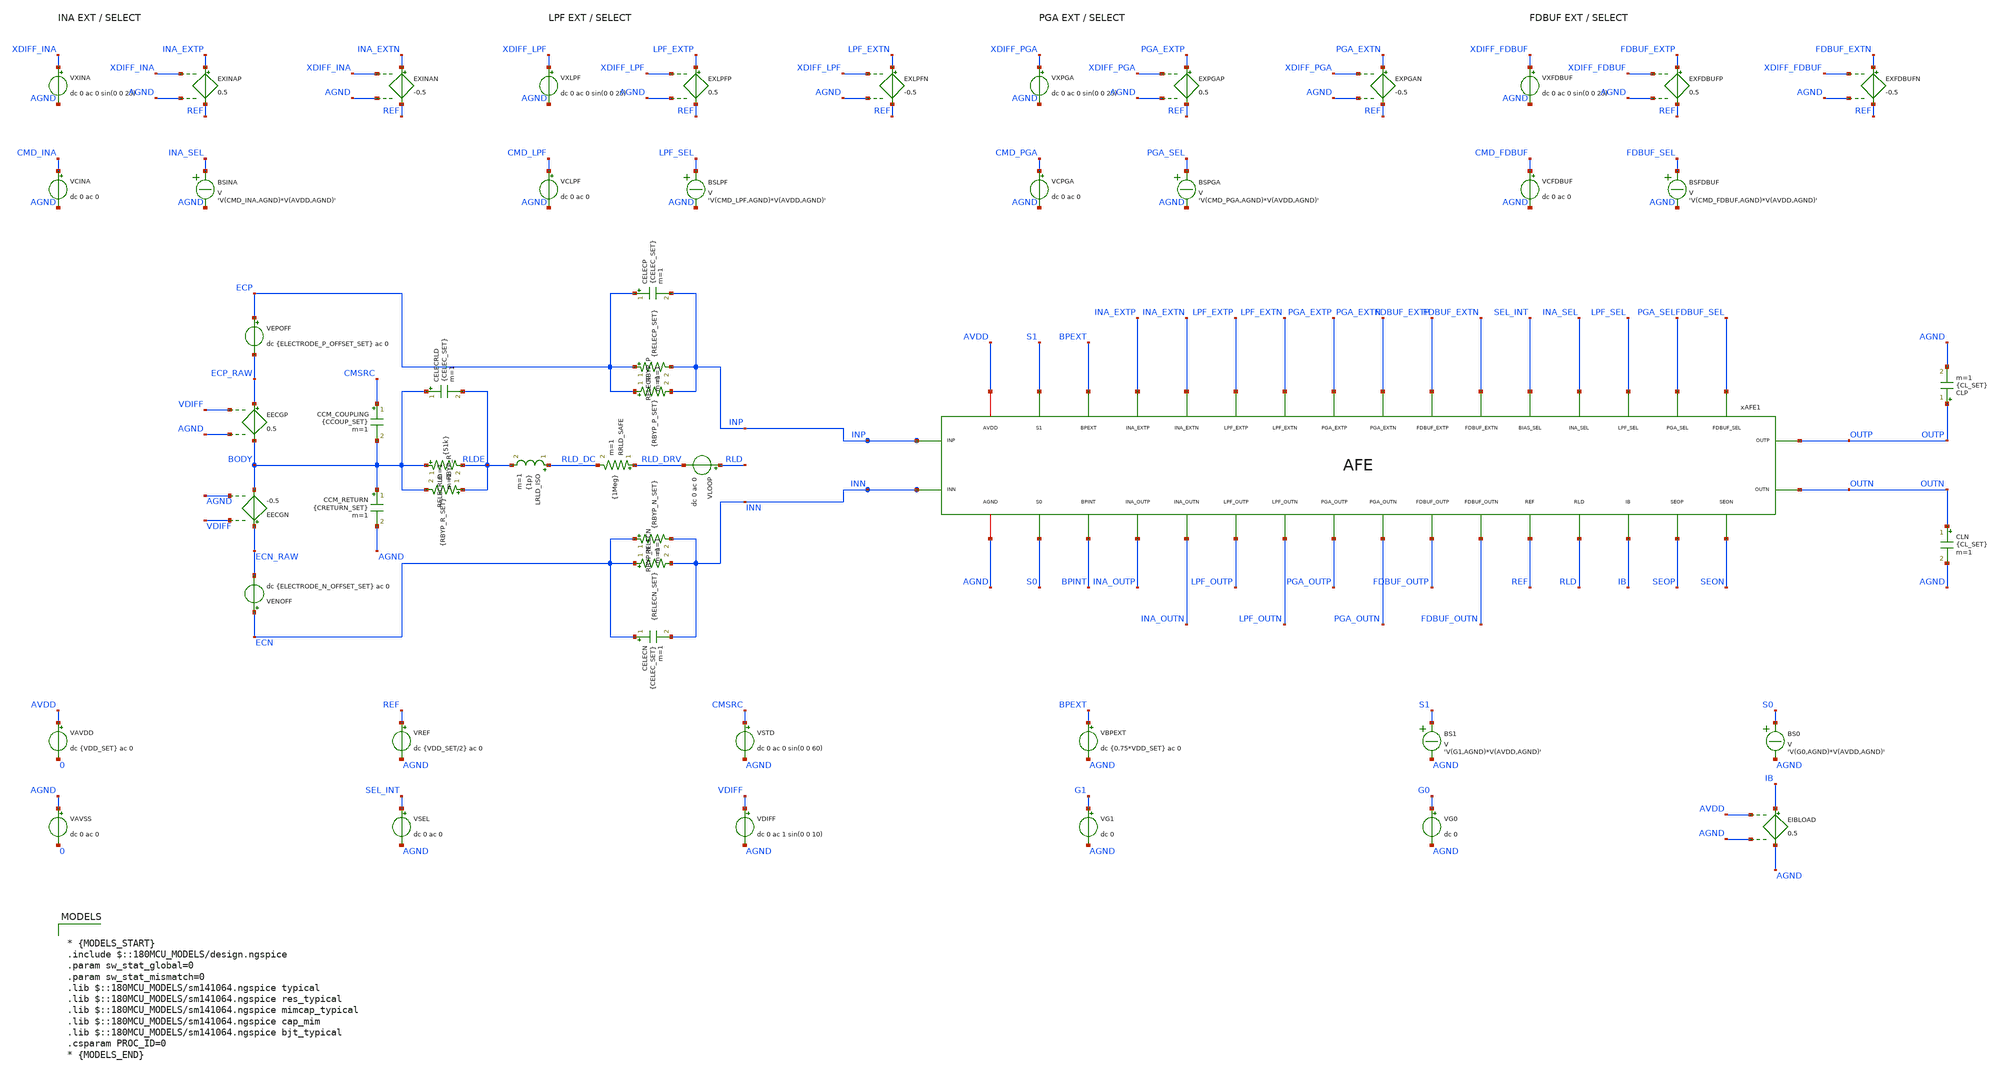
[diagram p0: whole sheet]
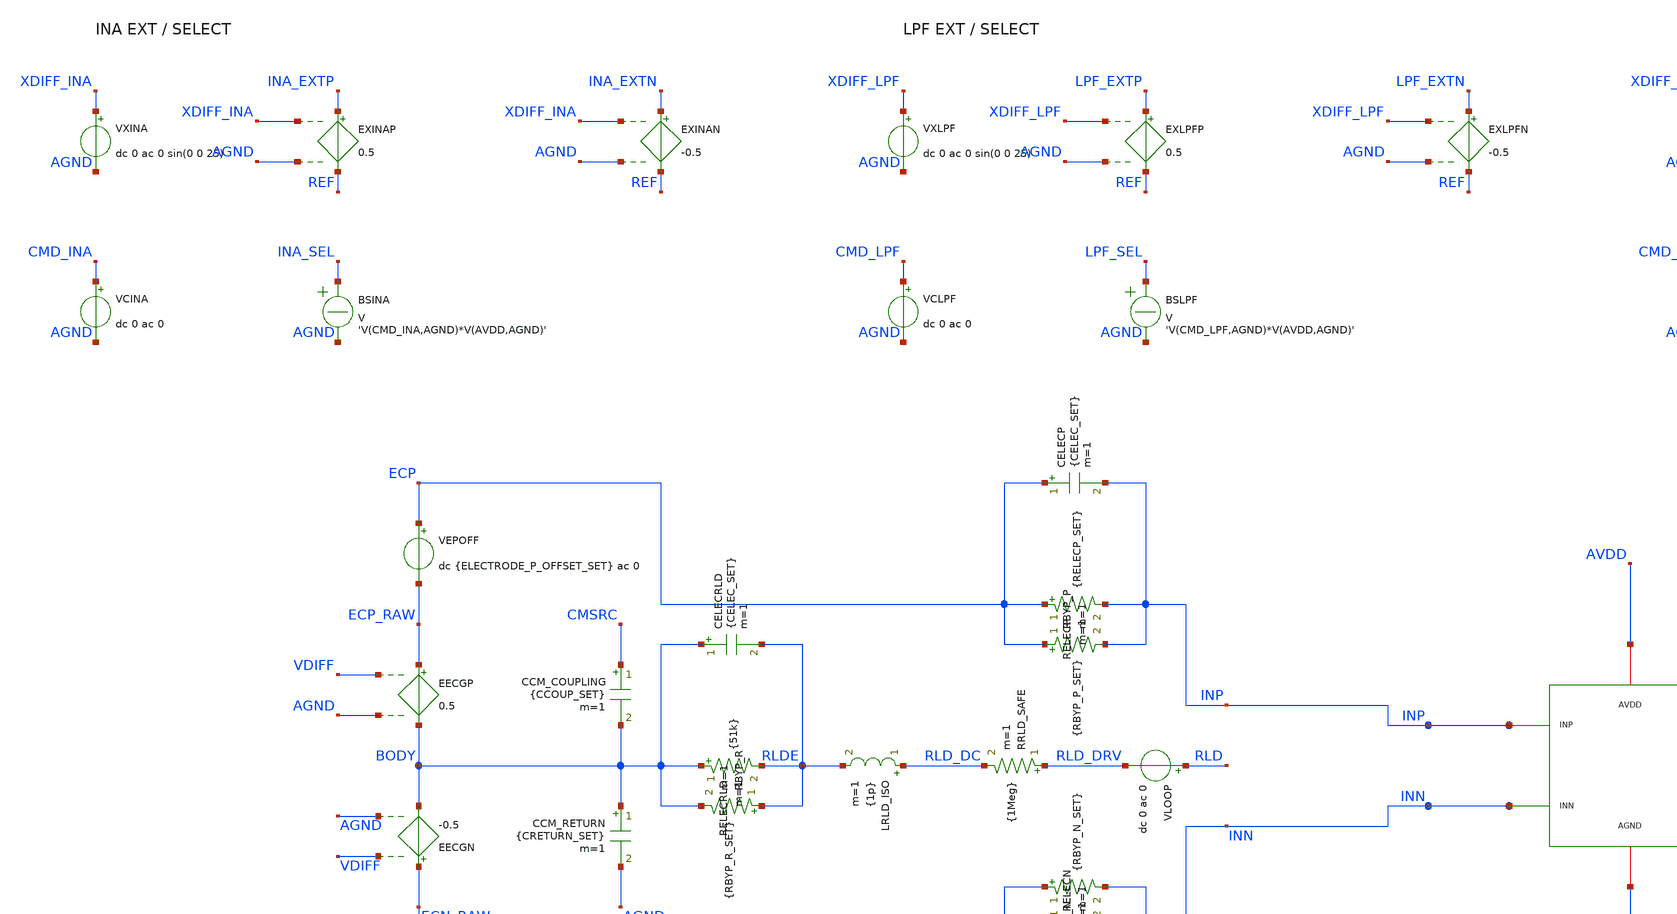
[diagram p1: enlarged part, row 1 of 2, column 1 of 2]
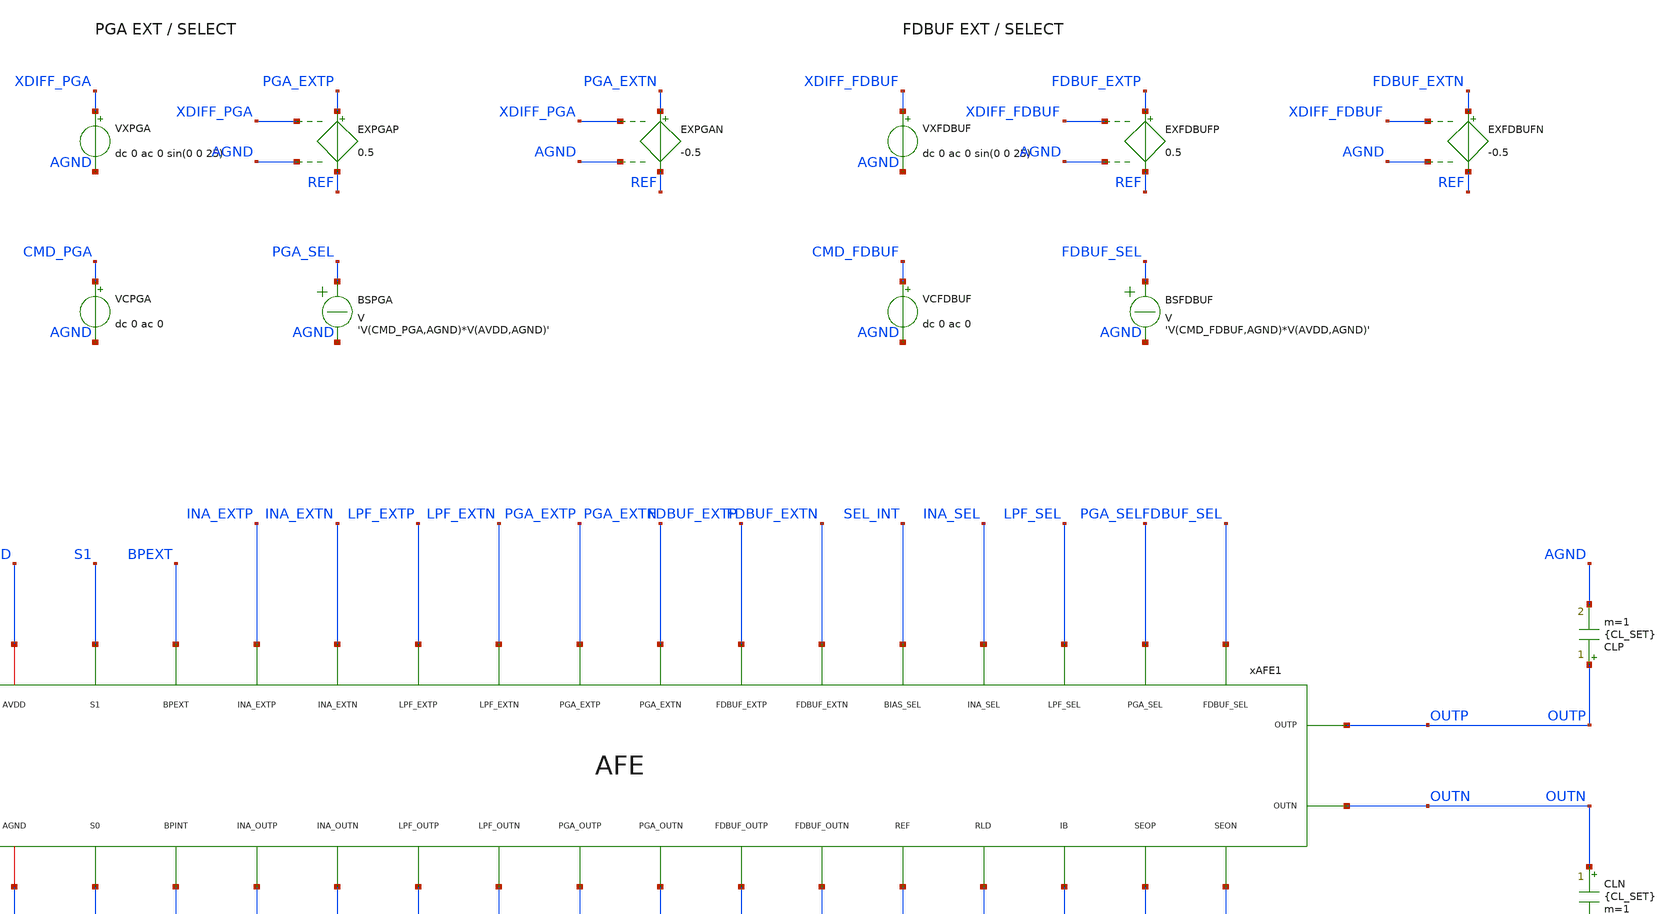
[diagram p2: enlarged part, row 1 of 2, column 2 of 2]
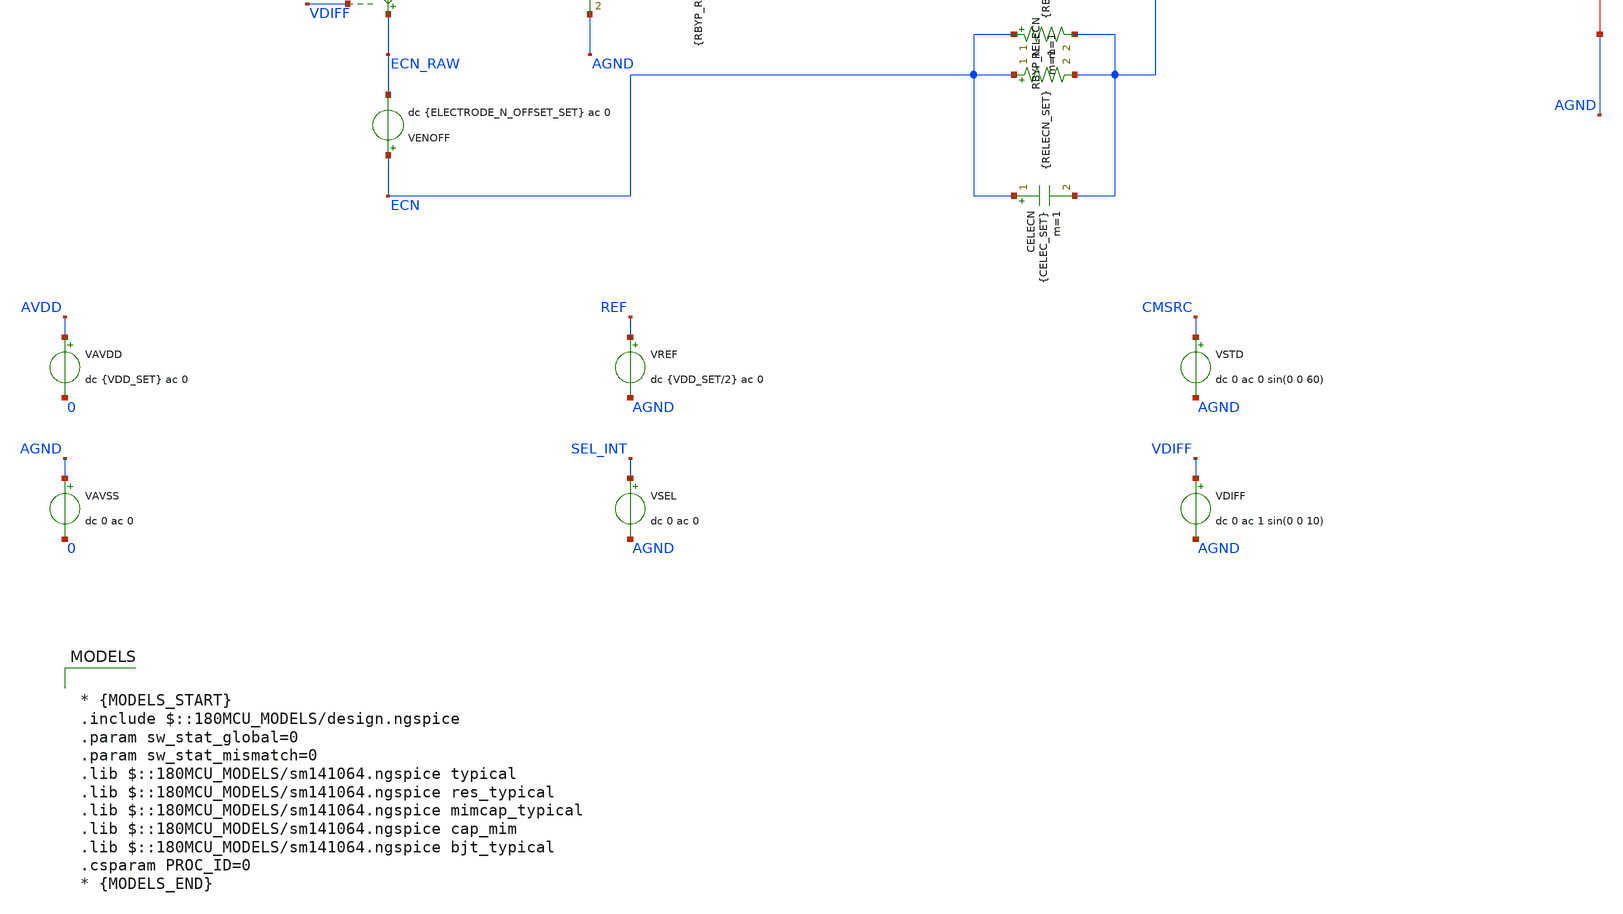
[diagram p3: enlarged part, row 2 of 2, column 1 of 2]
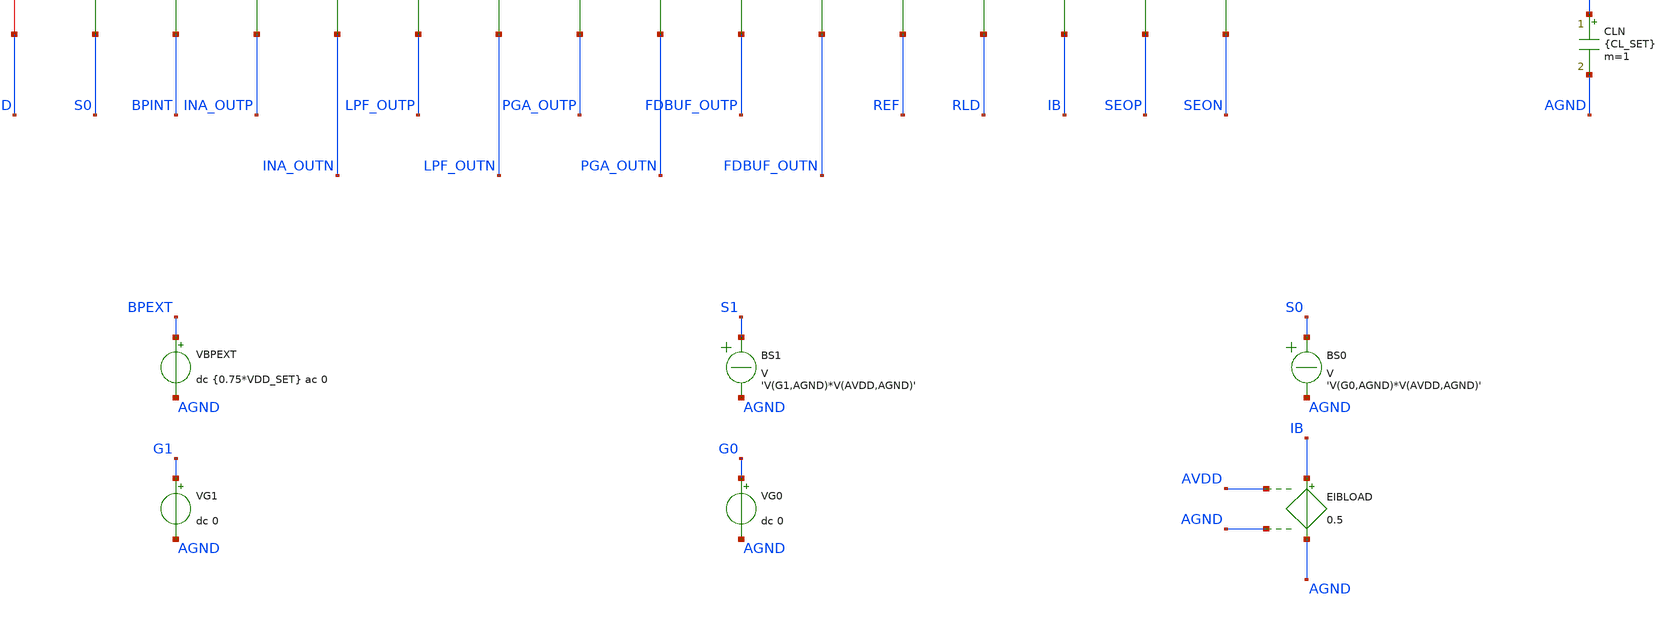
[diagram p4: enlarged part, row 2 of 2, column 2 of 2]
** sch_path: Design_Files/IC Design/Testbench/AFE_BLOCKS/AFE/AFE_TB_PVT_NOM.sch
**.subckt AFE_TB_PVT_NOM
VXINA XDIFF_INA AGND dc 0 ac 0 sin(0 0 25)
EXINAP INA_EXTP REF XDIFF_INA AGND 0.5
EXINAN INA_EXTN REF XDIFF_INA AGND -0.5
VCINA CMD_INA AGND dc 0 ac 0
BSINA INA_SEL AGND V = 'V(CMD_INA,AGND)*V(AVDD,AGND)'
VXLPF XDIFF_LPF AGND dc 0 ac 0 sin(0 0 25)
EXLPFP LPF_EXTP REF XDIFF_LPF AGND 0.5
EXLPFN LPF_EXTN REF XDIFF_LPF AGND -0.5
VCLPF CMD_LPF AGND dc 0 ac 0
BSLPF LPF_SEL AGND V = 'V(CMD_LPF,AGND)*V(AVDD,AGND)'
VXPGA XDIFF_PGA AGND dc 0 ac 0 sin(0 0 25)
EXPGAP PGA_EXTP REF XDIFF_PGA AGND 0.5
EXPGAN PGA_EXTN REF XDIFF_PGA AGND -0.5
VCPGA CMD_PGA AGND dc 0 ac 0
BSPGA PGA_SEL AGND V = 'V(CMD_PGA,AGND)*V(AVDD,AGND)'
VXFDBUF XDIFF_FDBUF AGND dc 0 ac 0 sin(0 0 25)
EXFDBUFP FDBUF_EXTP REF XDIFF_FDBUF AGND 0.5
EXFDBUFN FDBUF_EXTN REF XDIFF_FDBUF AGND -0.5
VCFDBUF CMD_FDBUF AGND dc 0 ac 0
BSFDBUF FDBUF_SEL AGND V = 'V(CMD_FDBUF,AGND)*V(AVDD,AGND)'
EECGP ECP_RAW BODY VDIFF AGND 0.5
EECGN ECN_RAW BODY VDIFF AGND -0.5
VLOOP RLD RLD_DRV dc 0 ac 0
.save i(vloop)
CCM_COUPLING CMSRC BODY {CCOUP_SET} m=1
RELECP ECP INP {RELECP_SET} m=1
RELECN ECN INN {RELECN_SET} m=1
CELECP ECP INP {CELEC_SET} m=1
CELECN ECN INN {CELEC_SET} m=1
RRLD_SAFE RLD_DRV RLD_DC {1Meg} m=1
RELECRLD BODY RLDE {51k} m=1
CELECRLD BODY RLDE {CELEC_SET} m=1
VEPOFF ECP ECP_RAW dc {ELECTRODE_P_OFFSET_SET} ac 0
VENOFF ECN ECN_RAW dc {ELECTRODE_N_OFFSET_SET} ac 0
CCM_RETURN BODY AGND {CRETURN_SET} m=1
RBYP_P ECP INP {RBYP_P_SET} m=1
RBYP_N ECN INN {RBYP_N_SET} m=1
RBYP_R RLDE BODY {RBYP_R_SET} m=1
LRLD_ISO RLD_DC RLDE {1p} m=1
xAFE1 FDBUF_SEL LPF_SEL SEL_INT PGA_SEL AVDD INA_SEL AGND FDBUF_OUTP BPINT LPF_OUTP PGA_OUTP
+ INA_OUTP INA_OUTN LPF_OUTN INP BPEXT FDBUF_OUTN PGA_OUTN FDBUF_EXTP LPF_EXTP INN PGA_EXTP INA_EXTP PGA_EXTN
+ INA_EXTN FDBUF_EXTN LPF_EXTN OUTP REF OUTN S1 SEOP IB S0 SEON RLD AFE
VAVDD AVDD 0 dc {VDD_SET} ac 0
.save i(vavdd)
VAVSS AGND 0 dc 0 ac 0
VREF REF AGND dc {VDD_SET/2} ac 0
VSEL SEL_INT AGND dc 0 ac 0
VSTD CMSRC AGND dc 0 ac 0 sin(0 0 60)
VDIFF VDIFF AGND dc 0 ac 1 sin(0 0 10)
VBPEXT BPEXT AGND dc {0.75*VDD_SET} ac 0
VG1 G1 AGND dc 0
VG0 G0 AGND dc 0
BS1 S1 AGND V = 'V(G1,AGND)*V(AVDD,AGND)'
BS0 S0 AGND V = 'V(G0,AGND)*V(AVDD,AGND)'
CLP OUTP AGND {CL_SET} m=1
CLN OUTN AGND {CL_SET} m=1
EIBLOAD IB AGND AVDD AGND 0.5
**** begin user architecture code

* {MODELS_START}
.include $::180MCU_MODELS/design.ngspice
.param sw_stat_global=0
.param sw_stat_mismatch=0
.lib $::180MCU_MODELS/sm141064.ngspice typical
.lib $::180MCU_MODELS/sm141064.ngspice res_typical
.lib $::180MCU_MODELS/sm141064.ngspice mimcap_typical
.lib $::180MCU_MODELS/sm141064.ngspice cap_mim
.lib $::180MCU_MODELS/sm141064.ngspice bjt_typical
.csparam PROC_ID=0
* {MODELS_END}




* {SETUP_START}
.param VDD_SET=3.3
.param TEMP_SET=27
.param CL_SET=60p
.param RELECP_SET=51k
.param RELECN_SET=51k
.param CELEC_SET=47n
.param CCOUP_SET=100p
.param CRETURN_SET=100p
.param ELECTRODE_P_OFFSET_SET=0
.param ELECTRODE_N_OFFSET_SET=0
.param RBYP_P_SET=1e15
.param RBYP_N_SET=1e15
.param RBYP_R_SET=1e15
.csparam MC_RUNS=200
* Target final differential sine amplitude = 1 V peak, f0 = 10 Hz.
* Coherent FFT: settle 0.2 s; record 0.4 s (4 cycles); N=4096.
* Export resampled record including endpoint; FFT reader must discard last point.
.temp {TEMP_SET}
.options gmin=1e-12 rshunt=1e12 method=gear
* {SETUP_END}





* {MEAS_START}
.control
destroy all
set noaskquit
set wr_singlescale
unset wr_vecnames
option klu
option numdgt=15
option method=gear
option maxord=2
option plotwinsize=0

if $&PROC_ID = 0
setcs proc=NOM
end
if $&PROC_ID = 1
setcs proc=FF
end
if $&PROC_ID = 2
setcs proc=SS
end
if $&PROC_ID = 3
setcs proc=FS
end
if $&PROC_ID = 4
setcs proc=SF
end
setcs outdir=/foss/designs/ECG_Acquisition_IC/Measurement_Results/IC_Simulation/AFE_BLOCKS/AFE/{$proc}.Result_txt
shell mkdir -p {$outdir}
* Existing exports are not removed: an interrupted rerun must not erase results.
foreach ecode 0 1 2 3 4 5 6 7 8
set env=nom
set vddval=3.3
set tval=27
if $ecode = 1
set env=vl
set vddval=3
set tval=27
end
if $ecode = 2
set env=vh
set vddval=3.6
set tval=27
end
if $ecode = 3
set env=tl
set vddval=3.3
set tval=-40
end
if $ecode = 4
set env=th
set vddval=3.3
set tval=125
end
if $ecode = 5
set env=vltl
set vddval=3
set tval=-40
end
if $ecode = 6
set env=vlth
set vddval=3
set tval=125
end
if $ecode = 7
set env=vhtl
set vddval=3.6
set tval=-40
end
if $ecode = 8
set env=vhth
set vddval=3.6
set tval=125
end
alterparam VDD_SET=$vddval
alterparam TEMP_SET=$tval
reset
save all
save v(AVDD) v(AGND) v(REF) v(VDIFF) v(INP) v(INN) v(OUTP) v(OUTN) v(BODY) vavdd#branch
echo AFE PVT: $proc $env

* Identical measurement body in PVT and MC. No reset/mc_source inside gain loop.

* Normal performance always uses internal signal paths.
alter VCINA 0
alter VCLPF 0
alter VCPGA 0
alter VCFDBUF 0
alter @VXINA[acmag]=0
alter @VXLPF[acmag]=0
alter @VXPGA[acmag]=0
alter @VXFDBUF[acmag]=0

foreach gcode 0 1 2 3
alter VG1 0
alter VG0 0
if $gcode = 0
set gtag=g2
set gainval=480
end
if $gcode = 1
set gtag=g4
set gainval=960
alter VG0 1
end
if $gcode = 2
set gtag=g8
set gainval=1920
alter VG1 1
end
if $gcode = 3
set gtag=g16
set gainval=3840
alter VG1 1
alter VG0 1
end
setcs casefile={$outdir}/{$proc}.{$gtag}_{$env}
alter @VDIFF[sin] = [ 0 0 10 ]
alter @VDIFF[acmag]=0
alter @VSTD[sin] = [ 0 0 60 ]
alter @VSTD[acmag]=0
alter @VAVDD[acmag]=0
alter LRLD_ISO 1p
op
let idx=0
let vdd=v(AVDD)-v(AGND)
let idd=abs(vavdd#branch)
let power=vdd*idd
let outcm=0.5*(v(OUTP)+v(OUTN))-v(AGND)
let cmerr=outcm-v(REF)+v(AGND)
let outdiff=v(OUTP)-v(OUTN)
let incm=0.5*(v(INP)+v(INN))-v(AGND)
setscale idx
wrdata {$casefile}.op.txt vdd idd power cmerr outcm outdiff incm
destroy all

* Final differential gain includes electrode loading and integrated selectors.
alter @VDIFF[acmag]=1
ac dec 80 0.01 1Meg
let vin=v(VDIFF)-v(AGND)
let vout=v(OUTP)-v(OUTN)
let ir=real(vin)
let ii=imag(vin)
let yr=real(vout)
let yi=imag(vout)
wrdata {$casefile}.diff_ac.txt ir ii yr yi
destroy all

* Intrinsic chain CMRR: ideal equal common-mode drive at both electrodes.
* Body interference/RLD integration is measured separately below.
alter @VDIFF[acmag]=0
alter @VSTD[acmag]=1
ac dec 80 0.01 10k
let vin=0.5*(v(INP)+v(INN))-v(AGND)
let vout=v(OUTP)-v(OUTN)
let ir=real(vin)
let ii=imag(vin)
let yr=real(vout)
let yi=imag(vout)
wrdata {$casefile}.cmrr_ac.txt ir ii yr yi
destroy all
alter @VSTD[acmag]=0

alter @VAVDD[acmag]=1
ac dec 80 0.01 10k
let vsup=v(AVDD)-v(AGND)
let vout=v(OUTP)-v(OUTN)
let ir=real(vsup)
let ii=imag(vsup)
let yr=real(vout)
let yi=imag(vout)
wrdata {$casefile}.psrrp_ac.txt ir ii yr yi
destroy all
alter @VAVDD[acmag]=0

alter @VDIFF[acmag]=1
option sparse
noise v(OUTP,OUTN) VDIFF dec 100 0.01 1k
setplot previous
wrdata {$casefile}.noise.txt onoise_spectrum inoise_spectrum
destroy all
option klu

* No offset cancellation: saturation/clipping is a real integration result.
* Scale source amplitude to 1 V differential output peak at nominal gain.
let inputpk=1/$gainval
set amp=$&inputpk
alter @VDIFF[acmag]=0
alter @VDIFF[sin] = [ 0 $amp 10 ]
tran 97.65625u 600m 200m 97.65625u
linearize v(VDIFF) v(OUTP) v(OUTN) v(REF) v(AVDD)
let vd=v(VDIFF)
let op=v(OUTP)
let on=v(OUTN)
let ref=v(REF)
let vdd=v(AVDD)
wrdata {$casefile}.signal_tran.txt vd op on ref vdd
destroy all
alter @VDIFF[sin] = [ 0 0 10 ]

* RLD integration, same G2 and sample/corner as main measurements.
if $gcode = 0
foreach rcode 0 1
set rstate=on
alter LRLD_ISO 1p
if $rcode = 0
set rstate=off
alter LRLD_ISO 1e12
end
alter @VSTD[acmag]=1
ac dec 80 1 1k
let b=v(BODY)-v(AGND)
let incm=0.5*(v(INP)+v(INN))-v(AGND)
let yr=real(incm)
let yi=imag(incm)
let br=real(b)
let bi=imag(b)
* Unit source response; multiply by 20 Vrms for source-referenced CM residual.
wrdata {$casefile}.rld_{$rstate}_ac.txt yr yi br bi
destroy all
alter @VSTD[acmag]=0
* 20 Vrms mains source through 100 pF coupling, 60 Hz.
alter @VSTD[sin] = [ 0 28.2842712475 60 ]
tran 100u 400m 200m 100u
linearize v(BODY) v(INP) v(INN) v(OUTP) v(OUTN)
let body=v(BODY)
let incm=0.5*(v(INP)+v(INN))
let outdiff=v(OUTP)-v(OUTN)
wrdata {$casefile}.rld_{$rstate}_tran.txt body incm outdiff
destroy all
alter @VSTD[sin] = [ 0 0 60 ]
end
alter LRLD_ISO 1p
end
end

* SELECTOR INTEGRATION - G2, same corner/statistical realization.
* Independent 10 Hz main input and 25 Hz external input responses.
* EXT paths bypass upstream blocks: G2 targets are 2, 2, 1, 1 V/V.
alter VG1 0
alter VG0 0
alter LRLD_ISO 1p
alter @VDIFF[sin] = [ 0 0 10 ]
alter @VSTD[sin] = [ 0 0 60 ]
alter @VSTD[acmag]=0
alter @VAVDD[acmag]=0
foreach pcode 0 1 2 3
if $pcode = 0
set path=ina
set xtarget=2
end
if $pcode = 1
set path=lpf
set xtarget=2
end
if $pcode = 2
set path=pga
set xtarget=1
end
if $pcode = 3
set path=fdbuf
set xtarget=1
end
foreach scode 0 1
set selection=int
if $scode = 1
set selection=ext
end
alter VCINA 0
alter VCLPF 0
alter VCPGA 0
alter VCFDBUF 0
if $scode = 1
if $pcode = 0
alter VCINA 1
end
if $pcode = 1
alter VCLPF 1
end
if $pcode = 2
alter VCPGA 1
end
if $pcode = 3
alter VCFDBUF 1
end
end
alter @VDIFF[acmag]=0
alter @VXINA[acmag]=0
alter @VXLPF[acmag]=0
alter @VXPGA[acmag]=0
alter @VXFDBUF[acmag]=0
setcs sel_file={$outdir}/{$proc}.selector_{$path}_{$selection}_{$env}
op
let idx=0
let vdd=v(AVDD)-v(AGND)
let ref=v(REF)-v(AGND)
let op=v(OUTP)-v(AGND)
let on=v(OUTN)-v(AGND)
let mainpk=0.2/480
let extpk=0.3/$xtarget
setscale idx
wrdata {$sel_file}.op.txt vdd ref op on mainpk extpk
destroy all

* Main input transfer; actual state determines whether it is selected.
alter @VDIFF[acmag]=1
ac lin 1 10 10
let pr=real(v(OUTP)-v(AGND))
let pi=imag(v(OUTP)-v(AGND))
let nr=real(v(OUTN)-v(AGND))
let ni=imag(v(OUTN)-v(AGND))
wrdata {$sel_file}.main_ac.txt pr pi nr ni
destroy all
alter @VDIFF[acmag]=0

* Excite only the external pair belonging to this selector.
if $pcode = 0
alter @VXINA[acmag]=1
end
if $pcode = 1
alter @VXLPF[acmag]=1
end
if $pcode = 2
alter @VXPGA[acmag]=1
end
if $pcode = 3
alter @VXFDBUF[acmag]=1
end
ac lin 1 25 25
let pr=real(v(OUTP)-v(AGND))
let pi=imag(v(OUTP)-v(AGND))
let nr=real(v(OUTN)-v(AGND))
let ni=imag(v(OUTN)-v(AGND))
wrdata {$sel_file}.ext_ac.txt pr pi nr ni
destroy all
end
end
alter VCINA 0
alter VCLPF 0
alter VCPGA 0
alter VCFDBUF 0
alter @VXINA[acmag]=0
alter @VXLPF[acmag]=0
alter @VXPGA[acmag]=0
alter @VXFDBUF[acmag]=0

end
quit
.endc
* {MEAS_END}


**** end user architecture code
**.ends
.end
